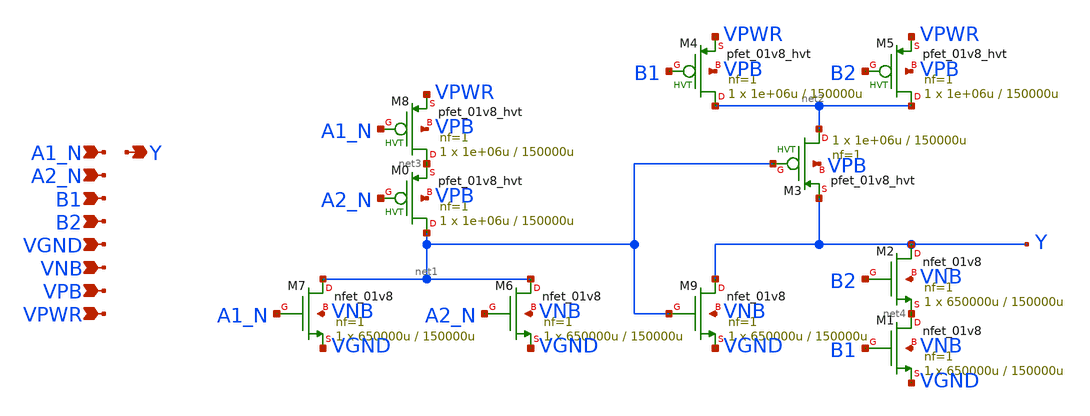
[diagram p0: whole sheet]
** sch_path: schematics/a2bb2oi/sky130_fd_sc_hd__a2bb2oi_1.sch
**.subckt sky130_fd_sc_hd__a2bb2oi_1 A1_N A2_N B1 B2 VGND VNB VPB VPWR Y
*.ipin A1_N
*.ipin A2_N
*.ipin B1
*.ipin B2
*.ipin VGND
*.ipin VNB
*.ipin VPB
*.ipin VPWR
*.opin Y
XM8 net3 A1_N VPWR VPB sky130_fd_pr__pfet_01v8_hvt L=150000u W=1e+06u nf=1 ad='int((1 + 1)/2) * 1e+06u / 1 * 0.29'
+ as='int((1 + 2)/2) * 1e+06u / 1 * 0.29' pd='2*int((1 + 1)/2) * (1e+06u / 1 + 0.29)' ps='2*int((1 + 2)/2) * (1e+06u / 1 + 0.29)'
+ nrd='0.29 / 1e+06u ' nrs='0.29 / 1e+06u ' sa=0 sb=0 sd=0 mult=1 m=1
XM0 net1 A2_N net3 VPB sky130_fd_pr__pfet_01v8_hvt L=150000u W=1e+06u nf=1 ad='int((1 + 1)/2) * 1e+06u / 1 * 0.29'
+ as='int((1 + 2)/2) * 1e+06u / 1 * 0.29' pd='2*int((1 + 1)/2) * (1e+06u / 1 + 0.29)' ps='2*int((1 + 2)/2) * (1e+06u / 1 + 0.29)'
+ nrd='0.29 / 1e+06u ' nrs='0.29 / 1e+06u ' sa=0 sb=0 sd=0 mult=1 m=1
XM3 net2 net1 Y VPB sky130_fd_pr__pfet_01v8_hvt L=150000u W=1e+06u nf=1 ad='int((1 + 1)/2) * 1e+06u / 1 * 0.29'
+ as='int((1 + 2)/2) * 1e+06u / 1 * 0.29' pd='2*int((1 + 1)/2) * (1e+06u / 1 + 0.29)' ps='2*int((1 + 2)/2) * (1e+06u / 1 + 0.29)'
+ nrd='0.29 / 1e+06u ' nrs='0.29 / 1e+06u ' sa=0 sb=0 sd=0 mult=1 m=1
XM4 net2 B1 VPWR VPB sky130_fd_pr__pfet_01v8_hvt L=150000u W=1e+06u nf=1 ad='int((1 + 1)/2) * 1e+06u / 1 * 0.29'
+ as='int((1 + 2)/2) * 1e+06u / 1 * 0.29' pd='2*int((1 + 1)/2) * (1e+06u / 1 + 0.29)' ps='2*int((1 + 2)/2) * (1e+06u / 1 + 0.29)'
+ nrd='0.29 / 1e+06u ' nrs='0.29 / 1e+06u ' sa=0 sb=0 sd=0 mult=1 m=1
XM5 net2 B2 VPWR VPB sky130_fd_pr__pfet_01v8_hvt L=150000u W=1e+06u nf=1 ad='int((1 + 1)/2) * 1e+06u / 1 * 0.29'
+ as='int((1 + 2)/2) * 1e+06u / 1 * 0.29' pd='2*int((1 + 1)/2) * (1e+06u / 1 + 0.29)' ps='2*int((1 + 2)/2) * (1e+06u / 1 + 0.29)'
+ nrd='0.29 / 1e+06u ' nrs='0.29 / 1e+06u ' sa=0 sb=0 sd=0 mult=1 m=1
XM7 net1 A1_N VGND VNB sky130_fd_pr__nfet_01v8 L=150000u W=650000u nf=1 ad='int((1 + 1)/2) * 650000u / 1 * 0.29'
+ as='int((1 + 2)/2) * 650000u / 1 * 0.29' pd='2*int((1 + 1)/2) * (650000u / 1 + 0.29)' ps='2*int((1 + 2)/2) * (650000u / 1 + 0.29)'
+ nrd='0.29 / 650000u ' nrs='0.29 / 650000u ' sa=0 sb=0 sd=0 mult=1 m=1
XM6 net1 A2_N VGND VNB sky130_fd_pr__nfet_01v8 L=150000u W=650000u nf=1 ad='int((1 + 1)/2) * 650000u / 1 * 0.29'
+ as='int((1 + 2)/2) * 650000u / 1 * 0.29' pd='2*int((1 + 1)/2) * (650000u / 1 + 0.29)' ps='2*int((1 + 2)/2) * (650000u / 1 + 0.29)'
+ nrd='0.29 / 650000u ' nrs='0.29 / 650000u ' sa=0 sb=0 sd=0 mult=1 m=1
XM9 Y net1 VGND VNB sky130_fd_pr__nfet_01v8 L=150000u W=650000u nf=1 ad='int((1 + 1)/2) * 650000u / 1 * 0.29'
+ as='int((1 + 2)/2) * 650000u / 1 * 0.29' pd='2*int((1 + 1)/2) * (650000u / 1 + 0.29)' ps='2*int((1 + 2)/2) * (650000u / 1 + 0.29)'
+ nrd='0.29 / 650000u ' nrs='0.29 / 650000u ' sa=0 sb=0 sd=0 mult=1 m=1
XM1 net4 B1 VGND VNB sky130_fd_pr__nfet_01v8 L=150000u W=650000u nf=1 ad='int((1 + 1)/2) * 650000u / 1 * 0.29'
+ as='int((1 + 2)/2) * 650000u / 1 * 0.29' pd='2*int((1 + 1)/2) * (650000u / 1 + 0.29)' ps='2*int((1 + 2)/2) * (650000u / 1 + 0.29)'
+ nrd='0.29 / 650000u ' nrs='0.29 / 650000u ' sa=0 sb=0 sd=0 mult=1 m=1
XM2 Y B2 net4 VNB sky130_fd_pr__nfet_01v8 L=150000u W=650000u nf=1 ad='int((1 + 1)/2) * 650000u / 1 * 0.29'
+ as='int((1 + 2)/2) * 650000u / 1 * 0.29' pd='2*int((1 + 1)/2) * (650000u / 1 + 0.29)' ps='2*int((1 + 2)/2) * (650000u / 1 + 0.29)'
+ nrd='0.29 / 650000u ' nrs='0.29 / 650000u ' sa=0 sb=0 sd=0 mult=1 m=1
**.ends
.end
